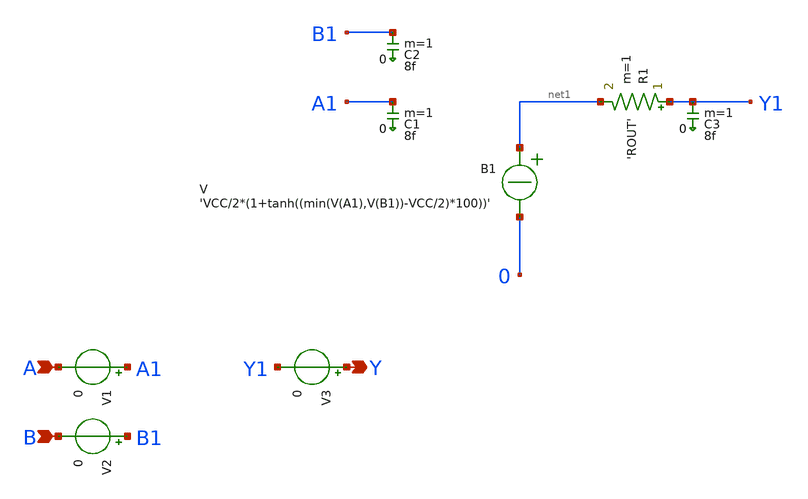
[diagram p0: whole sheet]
** sch_path: xschem_libraries_oa/ngspice/and_ngspice/schematic/and_ngspice.sch
* Copyright (C) 1998-2024 Stefan Frederik Schippers
* This program is free software; you can redistribute it and/or modify
* it under the terms of the GNU General Public License as published by
* the Free Software Foundation; either version 2 of the License, or
* (at your option) any later version.
* This program is distributed in the hope that it will be useful,
* but WITHOUT ANY WARRANTY; without even the implied warranty of
* MERCHANTABILITY or FITNESS FOR A PARTICULAR PURPOSE.  See the
* GNU General Public License for more details.
* You should have received a copy of the GNU General Public License
* along with this program; if not, write to the Free Software
**.subckt and_ngspice A Y B
*.ipin A
*.opin Y
*.ipin B
B1 net1 0 V = 'VCC/2*(1+tanh((min(V(A1),V(B1))-VCC/2)*100))'
R1 Y1 net1 'ROUT' m=1
C1 A1 0 8f m=1
C2 B1 0 8f m=1
C3 Y1 0 8f m=1
V1 A1 A 0
V2 B1 B 0
V3 Y Y1 0
**.ends
.end
